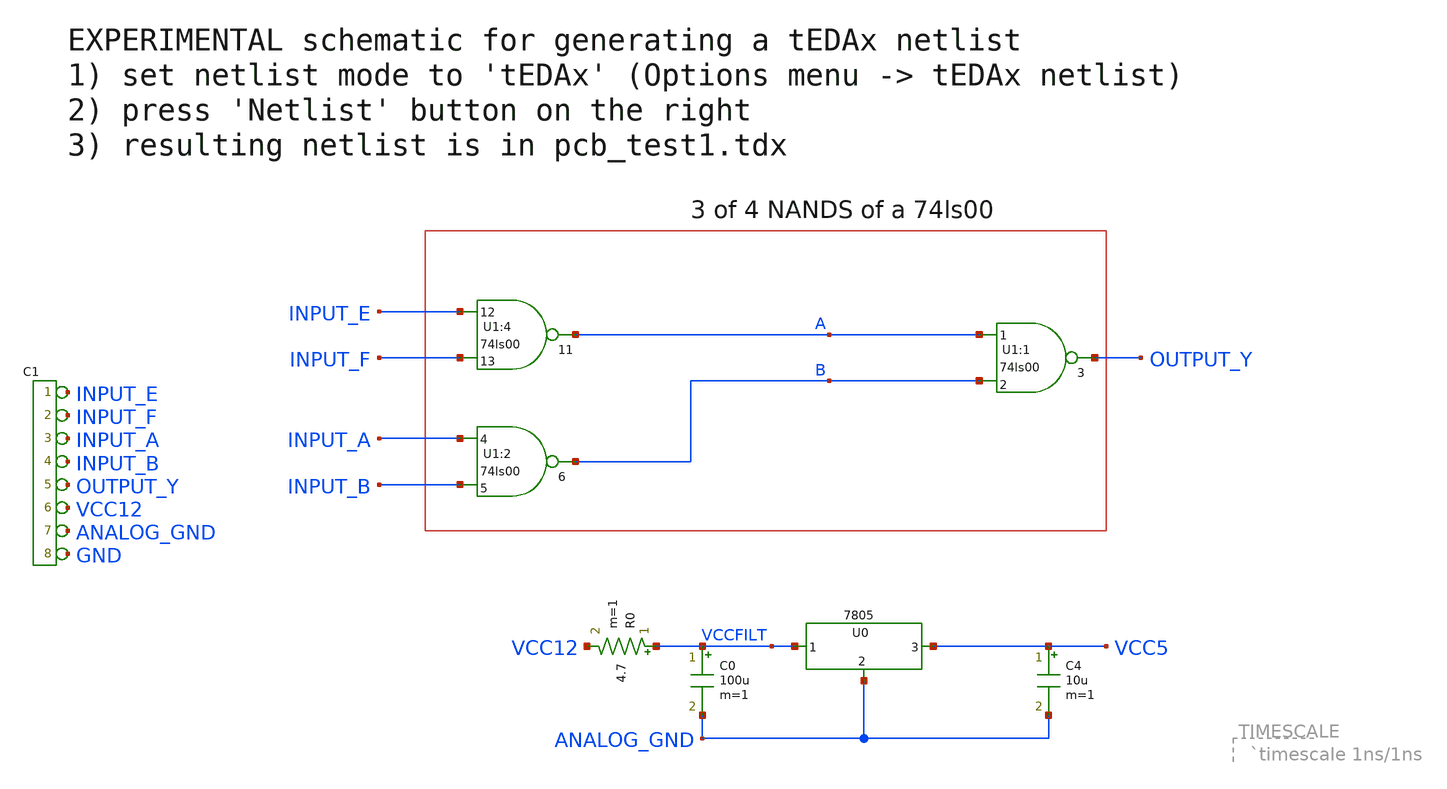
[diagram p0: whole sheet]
** sch_path: xschem_libs_newsym/pcb/pcb_test1_embed/schematic/pcb_test1_embed.sch
* Copyright (C) 1998-2024 Stefan Frederik Schippers
* This program is free software; you can redistribute it and/or modify
* it under the terms of the GNU General Public License as published by
* the Free Software Foundation; either version 2 of the License, or
* (at your option) any later version.
* This program is distributed in the hope that it will be useful,
* but WITHOUT ANY WARRANTY; without even the implied warranty of
* MERCHANTABILITY or FITNESS FOR A PARTICULAR PURPOSE.  See the
* GNU General Public License for more details.
* You should have received a copy of the GNU General Public License
* along with this program; if not, write to the Free Software
**.subckt pcb_test1_embed
U1:2 INPUT_A INPUT_B B
U1:1 A B OUTPUT_Y
C0 VCCFILT ANALOG_GND 100u m=1
U1:4 INPUT_E INPUT_F A
U0 VCCFILT ANALOG_GND VCC5 r7805
C4 VCC5 ANALOG_GND 10u m=1
R0 VCCFILT VCC12 4.7 m=1
*connector(8,1) ?1 INPUT_E ?1 INPUT_F ?1 INPUT_A ?1 INPUT_B ?1 OUTPUT_Y ?1 VCC12 ?1 ANALOG_GND ?1
*+ GND
**** begin user architecture code

initial begin
  $dumpfile("dumpfile.vcd");
  $dumpvars;
  INPUT_E=0;
  INPUT_F=0;
  INPUT_A=0;
  INPUT_B=0;
  ANALOG_GND=0;
  #10000;
  INPUT_A=1;
  INPUT_B=1;
  #10000;
  INPUT_E=1;
  INPUT_F=1;
  #10000;
  INPUT_F=0;
  #10000;
  INPUT_B=0;
  #10000;
  $finish;
end

assign VCC12=1;



**** end user architecture code
**.ends
.end
